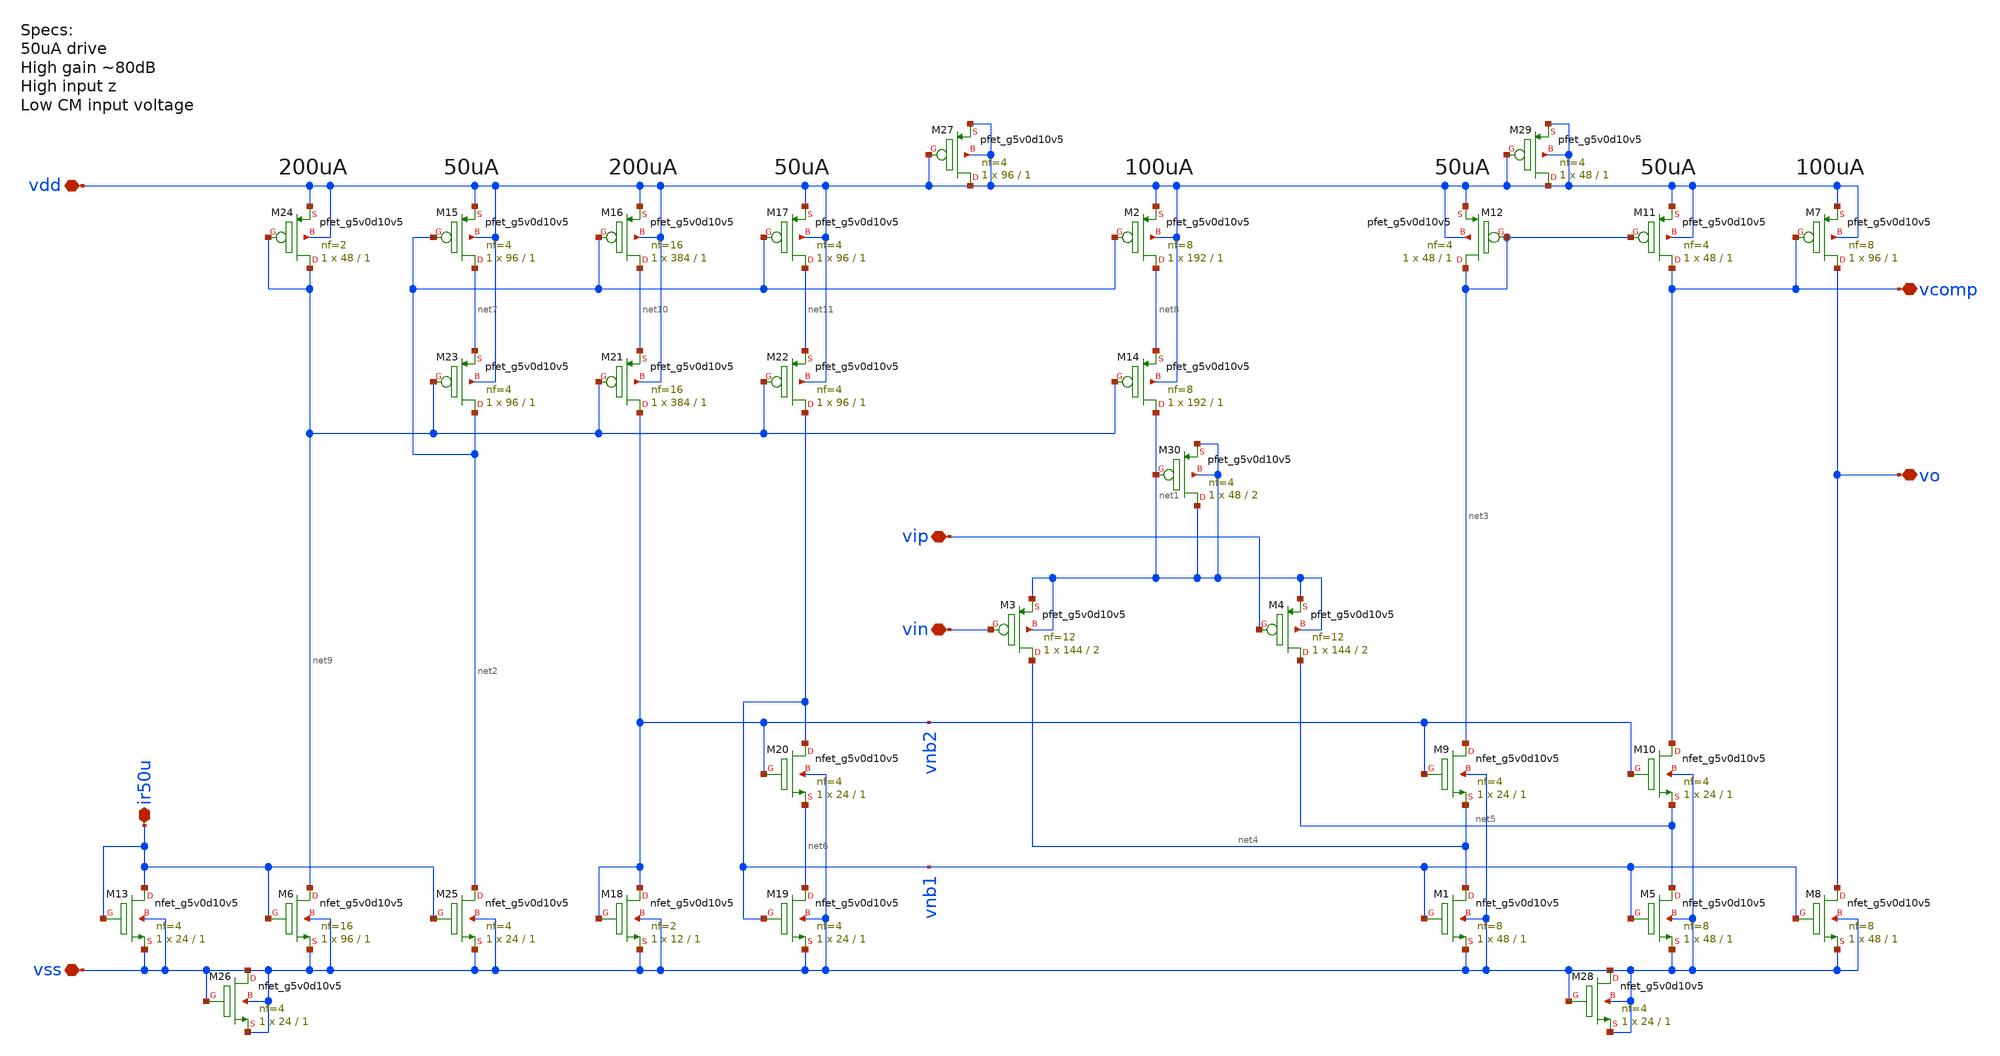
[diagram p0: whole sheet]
** sch_path: xschem/ip_block/opamp/folded_cas_high_swing/bgr_amp.sch
**.subckt bgr_amp vdd vss vcomp vip vin vo ir50u
*.iopin vdd
*.iopin vss
*.iopin vcomp
*.iopin vip
*.iopin vin
*.iopin vo
*.iopin ir50u
XM1 net4 vnb1 vss vss sky130_fd_pr__nfet_g5v0d10v5 L=1 W=48 nf=8 ad='int((nf+1)/2) * W/nf * 0.29' as='int((nf+2)/2) * W/nf * 0.29'
+ pd='2*int((nf+1)/2) * (W/nf + 0.29)' ps='2*int((nf+2)/2) * (W/nf + 0.29)' nrd='0.29 / W' nrs='0.29 / W'
+ sa=0 sb=0 sd=0 mult=1 m=1
XM2 net8 net2 vdd vdd sky130_fd_pr__pfet_g5v0d10v5 L=1 W=192 nf=8 ad='int((nf+1)/2) * W/nf * 0.29' as='int((nf+2)/2) * W/nf * 0.29'
+ pd='2*int((nf+1)/2) * (W/nf + 0.29)' ps='2*int((nf+2)/2) * (W/nf + 0.29)' nrd='0.29 / W' nrs='0.29 / W'
+ sa=0 sb=0 sd=0 mult=1 m=1
XM3 net4 vin net1 net1 sky130_fd_pr__pfet_g5v0d10v5 L=2 W=144 nf=12 ad='int((nf+1)/2) * W/nf * 0.29'
+ as='int((nf+2)/2) * W/nf * 0.29' pd='2*int((nf+1)/2) * (W/nf + 0.29)' ps='2*int((nf+2)/2) * (W/nf + 0.29)'
+ nrd='0.29 / W' nrs='0.29 / W' sa=0 sb=0 sd=0 mult=1 m=1
XM4 net5 vip net1 net1 sky130_fd_pr__pfet_g5v0d10v5 L=2 W=144 nf=12 ad='int((nf+1)/2) * W/nf * 0.29'
+ as='int((nf+2)/2) * W/nf * 0.29' pd='2*int((nf+1)/2) * (W/nf + 0.29)' ps='2*int((nf+2)/2) * (W/nf + 0.29)'
+ nrd='0.29 / W' nrs='0.29 / W' sa=0 sb=0 sd=0 mult=1 m=1
XM5 net5 vnb1 vss vss sky130_fd_pr__nfet_g5v0d10v5 L=1 W=48 nf=8 ad='int((nf+1)/2) * W/nf * 0.29' as='int((nf+2)/2) * W/nf * 0.29'
+ pd='2*int((nf+1)/2) * (W/nf + 0.29)' ps='2*int((nf+2)/2) * (W/nf + 0.29)' nrd='0.29 / W' nrs='0.29 / W'
+ sa=0 sb=0 sd=0 mult=1 m=1
XM7 vo vcomp vdd vdd sky130_fd_pr__pfet_g5v0d10v5 L=1 W=96 nf=8 ad='int((nf+1)/2) * W/nf * 0.29' as='int((nf+2)/2) * W/nf * 0.29'
+ pd='2*int((nf+1)/2) * (W/nf + 0.29)' ps='2*int((nf+2)/2) * (W/nf + 0.29)' nrd='0.29 / W' nrs='0.29 / W'
+ sa=0 sb=0 sd=0 mult=1 m=1
XM8 vo vnb1 vss vss sky130_fd_pr__nfet_g5v0d10v5 L=1 W=48 nf=8 ad='int((nf+1)/2) * W/nf * 0.29' as='int((nf+2)/2) * W/nf * 0.29'
+ pd='2*int((nf+1)/2) * (W/nf + 0.29)' ps='2*int((nf+2)/2) * (W/nf + 0.29)' nrd='0.29 / W' nrs='0.29 / W'
+ sa=0 sb=0 sd=0 mult=1 m=1
XM9 net3 vnb2 net4 vss sky130_fd_pr__nfet_g5v0d10v5 L=1 W=24 nf=4 ad='int((nf+1)/2) * W/nf * 0.29' as='int((nf+2)/2) * W/nf * 0.29'
+ pd='2*int((nf+1)/2) * (W/nf + 0.29)' ps='2*int((nf+2)/2) * (W/nf + 0.29)' nrd='0.29 / W' nrs='0.29 / W'
+ sa=0 sb=0 sd=0 mult=1 m=1
XM10 vcomp vnb2 net5 vss sky130_fd_pr__nfet_g5v0d10v5 L=1 W=24 nf=4 ad='int((nf+1)/2) * W/nf * 0.29'
+ as='int((nf+2)/2) * W/nf * 0.29' pd='2*int((nf+1)/2) * (W/nf + 0.29)' ps='2*int((nf+2)/2) * (W/nf + 0.29)'
+ nrd='0.29 / W' nrs='0.29 / W' sa=0 sb=0 sd=0 mult=1 m=1
XM11 vcomp net3 vdd vdd sky130_fd_pr__pfet_g5v0d10v5 L=1 W=48 nf=4 ad='int((nf+1)/2) * W/nf * 0.29' as='int((nf+2)/2) * W/nf * 0.29'
+ pd='2*int((nf+1)/2) * (W/nf + 0.29)' ps='2*int((nf+2)/2) * (W/nf + 0.29)' nrd='0.29 / W' nrs='0.29 / W'
+ sa=0 sb=0 sd=0 mult=1 m=1
XM12 net3 net3 vdd vdd sky130_fd_pr__pfet_g5v0d10v5 L=1 W=48 nf=4 ad='int((nf+1)/2) * W/nf * 0.29' as='int((nf+2)/2) * W/nf * 0.29'
+ pd='2*int((nf+1)/2) * (W/nf + 0.29)' ps='2*int((nf+2)/2) * (W/nf + 0.29)' nrd='0.29 / W' nrs='0.29 / W'
+ sa=0 sb=0 sd=0 mult=1 m=1
XM15 net7 net2 vdd vdd sky130_fd_pr__pfet_g5v0d10v5 L=1 W=96 nf=4 ad='int((nf+1)/2) * W/nf * 0.29' as='int((nf+2)/2) * W/nf * 0.29'
+ pd='2*int((nf+1)/2) * (W/nf + 0.29)' ps='2*int((nf+2)/2) * (W/nf + 0.29)' nrd='0.29 / W' nrs='0.29 / W'
+ sa=0 sb=0 sd=0 mult=1 m=1
XM16 net10 net2 vdd vdd sky130_fd_pr__pfet_g5v0d10v5 L=1 W=384 nf=16 ad='int((nf+1)/2) * W/nf * 0.29'
+ as='int((nf+2)/2) * W/nf * 0.29' pd='2*int((nf+1)/2) * (W/nf + 0.29)' ps='2*int((nf+2)/2) * (W/nf + 0.29)'
+ nrd='0.29 / W' nrs='0.29 / W' sa=0 sb=0 sd=0 mult=1 m=1
XM17 net11 net2 vdd vdd sky130_fd_pr__pfet_g5v0d10v5 L=1 W=96 nf=4 ad='int((nf+1)/2) * W/nf * 0.29' as='int((nf+2)/2) * W/nf * 0.29'
+ pd='2*int((nf+1)/2) * (W/nf + 0.29)' ps='2*int((nf+2)/2) * (W/nf + 0.29)' nrd='0.29 / W' nrs='0.29 / W'
+ sa=0 sb=0 sd=0 mult=1 m=1
XM18 vnb2 vnb2 vss vss sky130_fd_pr__nfet_g5v0d10v5 L=1 W=12 nf=2 ad='int((nf+1)/2) * W/nf * 0.29' as='int((nf+2)/2) * W/nf * 0.29'
+ pd='2*int((nf+1)/2) * (W/nf + 0.29)' ps='2*int((nf+2)/2) * (W/nf + 0.29)' nrd='0.29 / W' nrs='0.29 / W'
+ sa=0 sb=0 sd=0 mult=1 m=1
XM19 net6 vnb1 vss vss sky130_fd_pr__nfet_g5v0d10v5 L=1 W=24 nf=4 ad='int((nf+1)/2) * W/nf * 0.29' as='int((nf+2)/2) * W/nf * 0.29'
+ pd='2*int((nf+1)/2) * (W/nf + 0.29)' ps='2*int((nf+2)/2) * (W/nf + 0.29)' nrd='0.29 / W' nrs='0.29 / W'
+ sa=0 sb=0 sd=0 mult=1 m=1
XM20 vnb1 vnb2 net6 vss sky130_fd_pr__nfet_g5v0d10v5 L=1 W=24 nf=4 ad='int((nf+1)/2) * W/nf * 0.29' as='int((nf+2)/2) * W/nf * 0.29'
+ pd='2*int((nf+1)/2) * (W/nf + 0.29)' ps='2*int((nf+2)/2) * (W/nf + 0.29)' nrd='0.29 / W' nrs='0.29 / W'
+ sa=0 sb=0 sd=0 mult=1 m=1
XM6 net9 ir50u vss vss sky130_fd_pr__nfet_g5v0d10v5 L=1 W=96 nf=16 ad='int((nf+1)/2) * W/nf * 0.29' as='int((nf+2)/2) * W/nf * 0.29'
+ pd='2*int((nf+1)/2) * (W/nf + 0.29)' ps='2*int((nf+2)/2) * (W/nf + 0.29)' nrd='0.29 / W' nrs='0.29 / W'
+ sa=0 sb=0 sd=0 mult=1 m=1
XM13 ir50u ir50u vss vss sky130_fd_pr__nfet_g5v0d10v5 L=1 W=24 nf=4 ad='int((nf+1)/2) * W/nf * 0.29'
+ as='int((nf+2)/2) * W/nf * 0.29' pd='2*int((nf+1)/2) * (W/nf + 0.29)' ps='2*int((nf+2)/2) * (W/nf + 0.29)'
+ nrd='0.29 / W' nrs='0.29 / W' sa=0 sb=0 sd=0 mult=1 m=1
XM14 net1 net9 net8 vdd sky130_fd_pr__pfet_g5v0d10v5 L=1 W=192 nf=8 ad='int((nf+1)/2) * W/nf * 0.29'
+ as='int((nf+2)/2) * W/nf * 0.29' pd='2*int((nf+1)/2) * (W/nf + 0.29)' ps='2*int((nf+2)/2) * (W/nf + 0.29)'
+ nrd='0.29 / W' nrs='0.29 / W' sa=0 sb=0 sd=0 mult=1 m=1
XM21 vnb2 net9 net10 vdd sky130_fd_pr__pfet_g5v0d10v5 L=1 W=384 nf=16 ad='int((nf+1)/2) * W/nf * 0.29'
+ as='int((nf+2)/2) * W/nf * 0.29' pd='2*int((nf+1)/2) * (W/nf + 0.29)' ps='2*int((nf+2)/2) * (W/nf + 0.29)'
+ nrd='0.29 / W' nrs='0.29 / W' sa=0 sb=0 sd=0 mult=1 m=1
XM22 vnb1 net9 net11 vdd sky130_fd_pr__pfet_g5v0d10v5 L=1 W=96 nf=4 ad='int((nf+1)/2) * W/nf * 0.29'
+ as='int((nf+2)/2) * W/nf * 0.29' pd='2*int((nf+1)/2) * (W/nf + 0.29)' ps='2*int((nf+2)/2) * (W/nf + 0.29)'
+ nrd='0.29 / W' nrs='0.29 / W' sa=0 sb=0 sd=0 mult=1 m=1
XM23 net2 net9 net7 vdd sky130_fd_pr__pfet_g5v0d10v5 L=1 W=96 nf=4 ad='int((nf+1)/2) * W/nf * 0.29' as='int((nf+2)/2) * W/nf * 0.29'
+ pd='2*int((nf+1)/2) * (W/nf + 0.29)' ps='2*int((nf+2)/2) * (W/nf + 0.29)' nrd='0.29 / W' nrs='0.29 / W'
+ sa=0 sb=0 sd=0 mult=1 m=1
XM24 net9 net9 vdd vdd sky130_fd_pr__pfet_g5v0d10v5 L=1 W=48 nf=2 ad='int((nf+1)/2) * W/nf * 0.29' as='int((nf+2)/2) * W/nf * 0.29'
+ pd='2*int((nf+1)/2) * (W/nf + 0.29)' ps='2*int((nf+2)/2) * (W/nf + 0.29)' nrd='0.29 / W' nrs='0.29 / W'
+ sa=0 sb=0 sd=0 mult=1 m=1
XM25 net2 ir50u vss vss sky130_fd_pr__nfet_g5v0d10v5 L=1 W=24 nf=4 ad='int((nf+1)/2) * W/nf * 0.29' as='int((nf+2)/2) * W/nf * 0.29'
+ pd='2*int((nf+1)/2) * (W/nf + 0.29)' ps='2*int((nf+2)/2) * (W/nf + 0.29)' nrd='0.29 / W' nrs='0.29 / W'
+ sa=0 sb=0 sd=0 mult=1 m=1
XM26 vss vss vss vss sky130_fd_pr__nfet_g5v0d10v5 L=1 W=24 nf=4 ad='int((nf+1)/2) * W/nf * 0.29' as='int((nf+2)/2) * W/nf * 0.29'
+ pd='2*int((nf+1)/2) * (W/nf + 0.29)' ps='2*int((nf+2)/2) * (W/nf + 0.29)' nrd='0.29 / W' nrs='0.29 / W'
+ sa=0 sb=0 sd=0 mult=1 m=1
XM27 vdd vdd vdd vdd sky130_fd_pr__pfet_g5v0d10v5 L=1 W=96 nf=4 ad='int((nf+1)/2) * W/nf * 0.29' as='int((nf+2)/2) * W/nf * 0.29'
+ pd='2*int((nf+1)/2) * (W/nf + 0.29)' ps='2*int((nf+2)/2) * (W/nf + 0.29)' nrd='0.29 / W' nrs='0.29 / W'
+ sa=0 sb=0 sd=0 mult=1 m=1
XM28 vss vss vss vss sky130_fd_pr__nfet_g5v0d10v5 L=1 W=24 nf=4 ad='int((nf+1)/2) * W/nf * 0.29' as='int((nf+2)/2) * W/nf * 0.29'
+ pd='2*int((nf+1)/2) * (W/nf + 0.29)' ps='2*int((nf+2)/2) * (W/nf + 0.29)' nrd='0.29 / W' nrs='0.29 / W'
+ sa=0 sb=0 sd=0 mult=1 m=1
XM29 vdd vdd vdd vdd sky130_fd_pr__pfet_g5v0d10v5 L=1 W=48 nf=4 ad='int((nf+1)/2) * W/nf * 0.29' as='int((nf+2)/2) * W/nf * 0.29'
+ pd='2*int((nf+1)/2) * (W/nf + 0.29)' ps='2*int((nf+2)/2) * (W/nf + 0.29)' nrd='0.29 / W' nrs='0.29 / W'
+ sa=0 sb=0 sd=0 mult=1 m=1
XM30 net1 net1 net1 net1 sky130_fd_pr__pfet_g5v0d10v5 L=2 W=48 nf=4 ad='int((nf+1)/2) * W/nf * 0.29'
+ as='int((nf+2)/2) * W/nf * 0.29' pd='2*int((nf+1)/2) * (W/nf + 0.29)' ps='2*int((nf+2)/2) * (W/nf + 0.29)'
+ nrd='0.29 / W' nrs='0.29 / W' sa=0 sb=0 sd=0 mult=1 m=1
**.ends
.end
